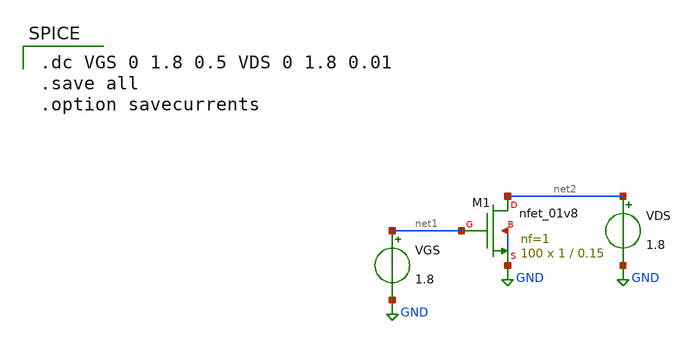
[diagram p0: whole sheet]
** sch_path: Spice_Files/pmos_DC.sch
**.subckt pmos_DC
XM1 net2 net1 GND GND sky130_fd_pr__nfet_01v8 L=0.15 W=1 nf=1 ad='int((nf+1)/2) * W/nf * 0.29' as='int((nf+2)/2) * W/nf * 0.29'
+ pd='2*int((nf+1)/2) * (W/nf + 0.29)' ps='2*int((nf+2)/2) * (W/nf + 0.29)' nrd='0.29 / W' nrs='0.29 / W'
+ sa=0 sb=0 sd=0 mult=100 m=100
VGS net1 GND 1.8
VDS net2 GND 1.8
**** begin user architecture code

.dc VGS 0 1.8 0.5 VDS 0 1.8 0.01
.save all
.option savecurrents

** manual skywater pdks install (with patches applied)
* .lib $::SKYWATER_MODELS/models/sky130.lib.spice tt_mm

** opencircuitdesign pdks install
.lib $::SKYWATER_MODELS/sky130.lib.spice tt_mm


**** end user architecture code
**.ends
.GLOBAL GND
.end
